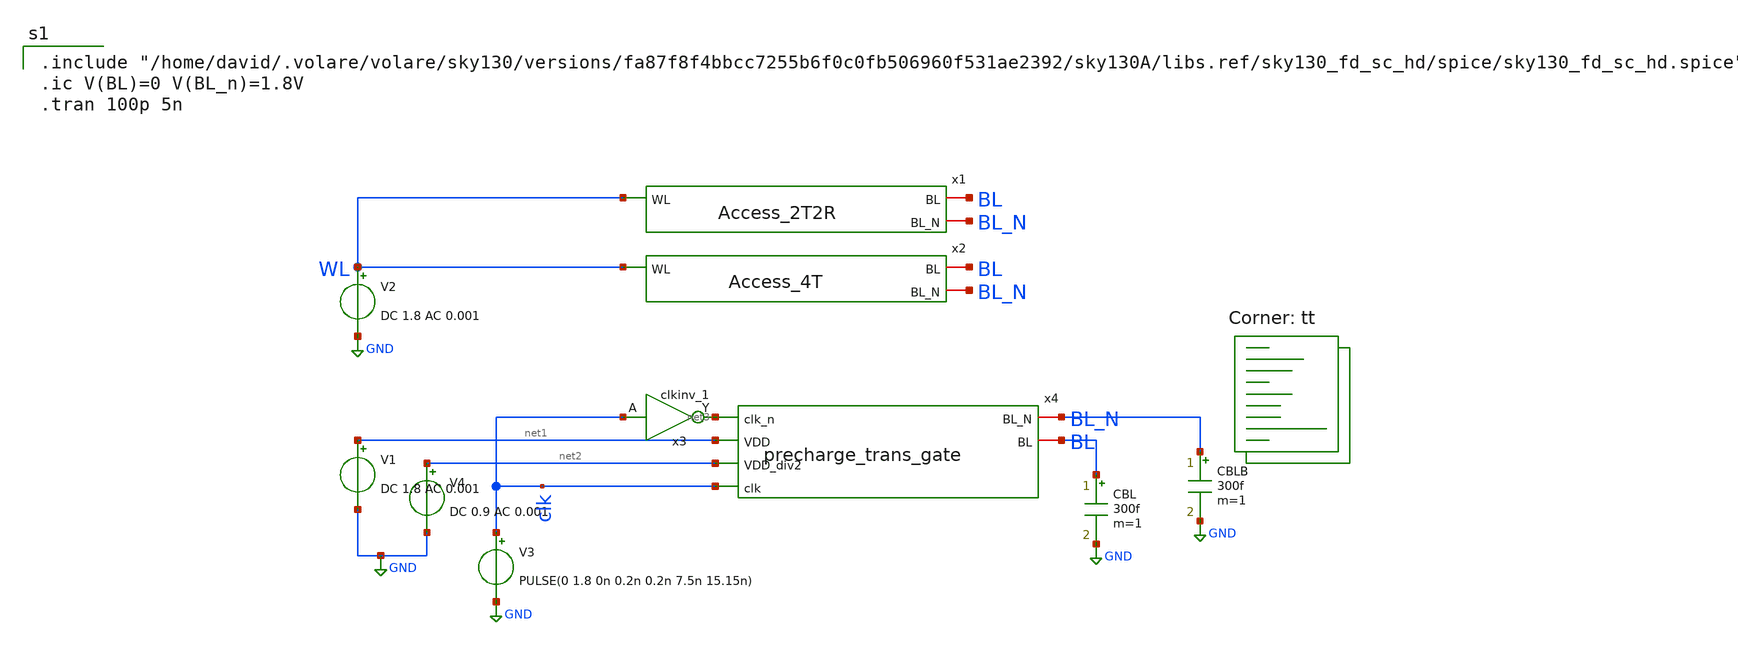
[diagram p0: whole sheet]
** sch_path: analog/schematics/Access_tb.sch
**.subckt Access_tb
x4 net3 BL_N BL net1 net2 clk precharge_trans_gate
V3 clk GND PULSE(0 1.8 0n 0.2n 0.2n 7.5n 15.15n)
x3 clk VGND VNB VPB VPWR net3 sky130_fd_sc_hd__clkinv_1
V4 net2 GND DC 0.9 AC 0.001
V1 net1 GND DC 1.8 AC 0.001
x1 WL BL BL_N Access_2T2R
x2 WL BL BL_N Access_4T
V2 WL GND DC 1.8 AC 0.001
CBLB BL_N GND 300f m=1
CBL BL GND 300f m=1
**** begin user architecture code

.include "/home/david/.volare/volare/sky130/versions/fa87f8f4bbcc7255b6f0c0fb506960f531ae2392/sky130A/libs.ref/sky130_fd_sc_hd/spice/sky130_fd_sc_hd.spice"
.ic V(BL)=0 V(BL_n)=1.8V
.tran 100p 5n

.lib $::SKYWATER_MODELS/sky130.lib.spice tt
**** end user architecture code
**.ends
.GLOBAL GND
.end
